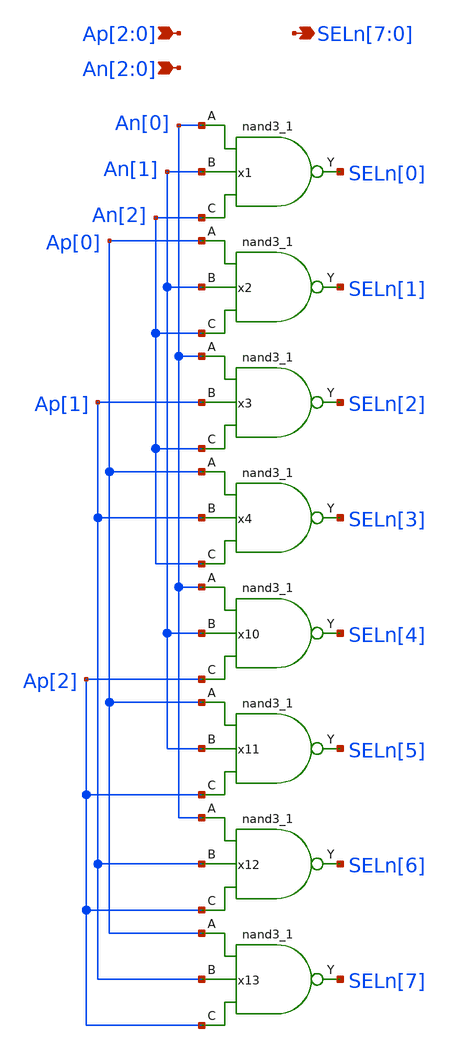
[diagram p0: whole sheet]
** sch_path: blocks/rom/rom_dec_3b.sch
**.subckt rom_dec_3b Ap[2],Ap[1],Ap[0]
*+ SELn[7],SELn[6],SELn[5],SELn[4],SELn[3],SELn[2],SELn[1],SELn[0] An[2],An[1],An[0]
*.ipin Ap[2],Ap[1],Ap[0]
*.opin SELn[7],SELn[6],SELn[5],SELn[4],SELn[3],SELn[2],SELn[1],SELn[0]
*.ipin An[2],An[1],An[0]
x1 An[0] An[1] An[2] VSS VSS VCC VCC SELn[0] sky130_fd_sc_hs__nand3_1
x2 Ap[0] An[1] An[2] VSS VSS VCC VCC SELn[1] sky130_fd_sc_hs__nand3_1
x3 An[0] Ap[1] An[2] VSS VSS VCC VCC SELn[2] sky130_fd_sc_hs__nand3_1
x4 Ap[0] Ap[1] An[2] VSS VSS VCC VCC SELn[3] sky130_fd_sc_hs__nand3_1
x10 An[0] An[1] Ap[2] VSS VSS VCC VCC SELn[4] sky130_fd_sc_hs__nand3_1
x11 Ap[0] An[1] Ap[2] VSS VSS VCC VCC SELn[5] sky130_fd_sc_hs__nand3_1
x12 An[0] Ap[1] Ap[2] VSS VSS VCC VCC SELn[6] sky130_fd_sc_hs__nand3_1
x13 Ap[0] Ap[1] Ap[2] VSS VSS VCC VCC SELn[7] sky130_fd_sc_hs__nand3_1
**.ends
.end
